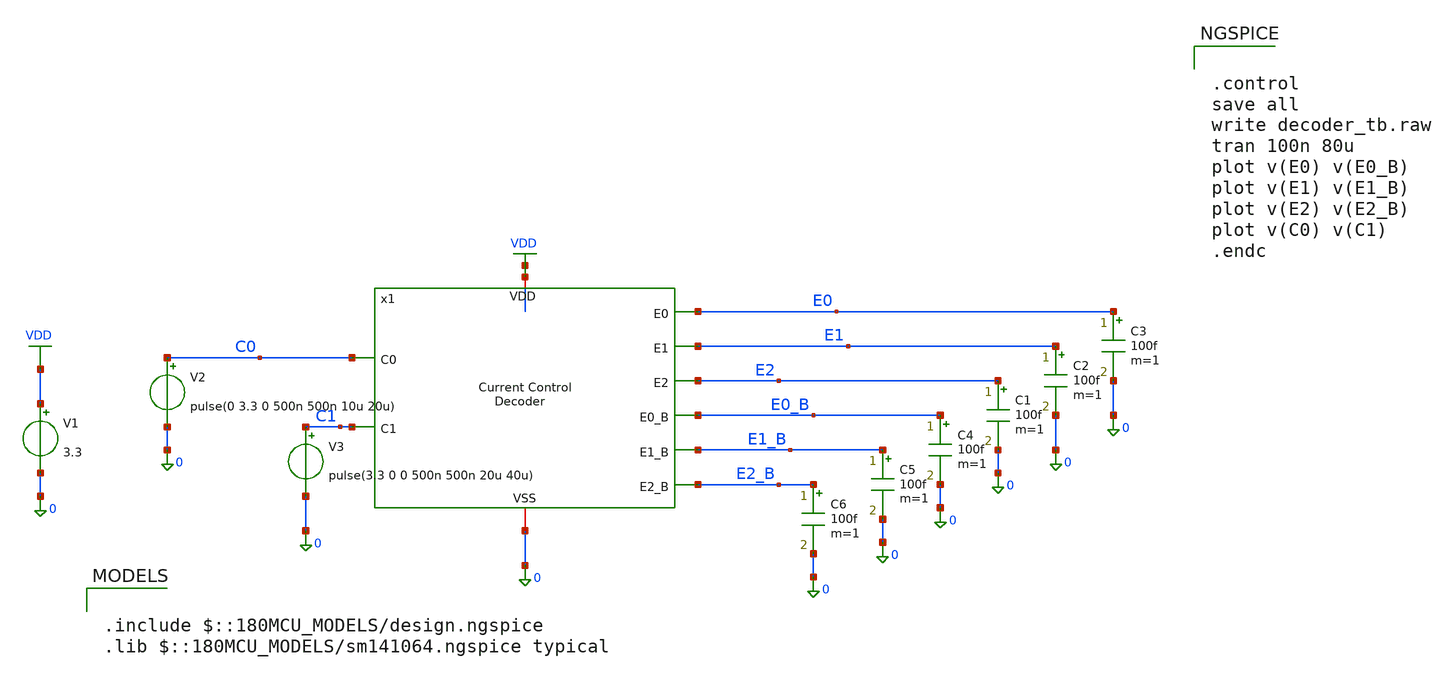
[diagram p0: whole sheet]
** sch_path: designs/digital/testbench/decoder_tb.sch
**.subckt decoder_tb
x1 net1 C0 E2 C1 0 E1 E0 E2_B E1_B E0_B decoder
V1 VDD 0 3.3
V2 C0 0 pulse(0 3.3 0 500n 500n 10u 20u)
V3 C1 0 pulse(3.3 0 0 500n 500n 20u 40u)
C1 E2 0 100f m=1
C2 E1 0 100f m=1
C3 E0 0 100f m=1
C4 E0_B 0 100f m=1
C5 E1_B 0 100f m=1
C6 E2_B 0 100f m=1
**** begin user architecture code

.include $::180MCU_MODELS/design.ngspice
.lib $::180MCU_MODELS/sm141064.ngspice typical



.control
save all
write decoder_tb.raw
tran 100n 80u
plot v(E0) v(E0_B)
plot v(E1) v(E1_B)
plot v(E2) v(E2_B)
plot v(C0) v(C1)
.endc


**** end user architecture code
**.ends
.GLOBAL VDD
.end
